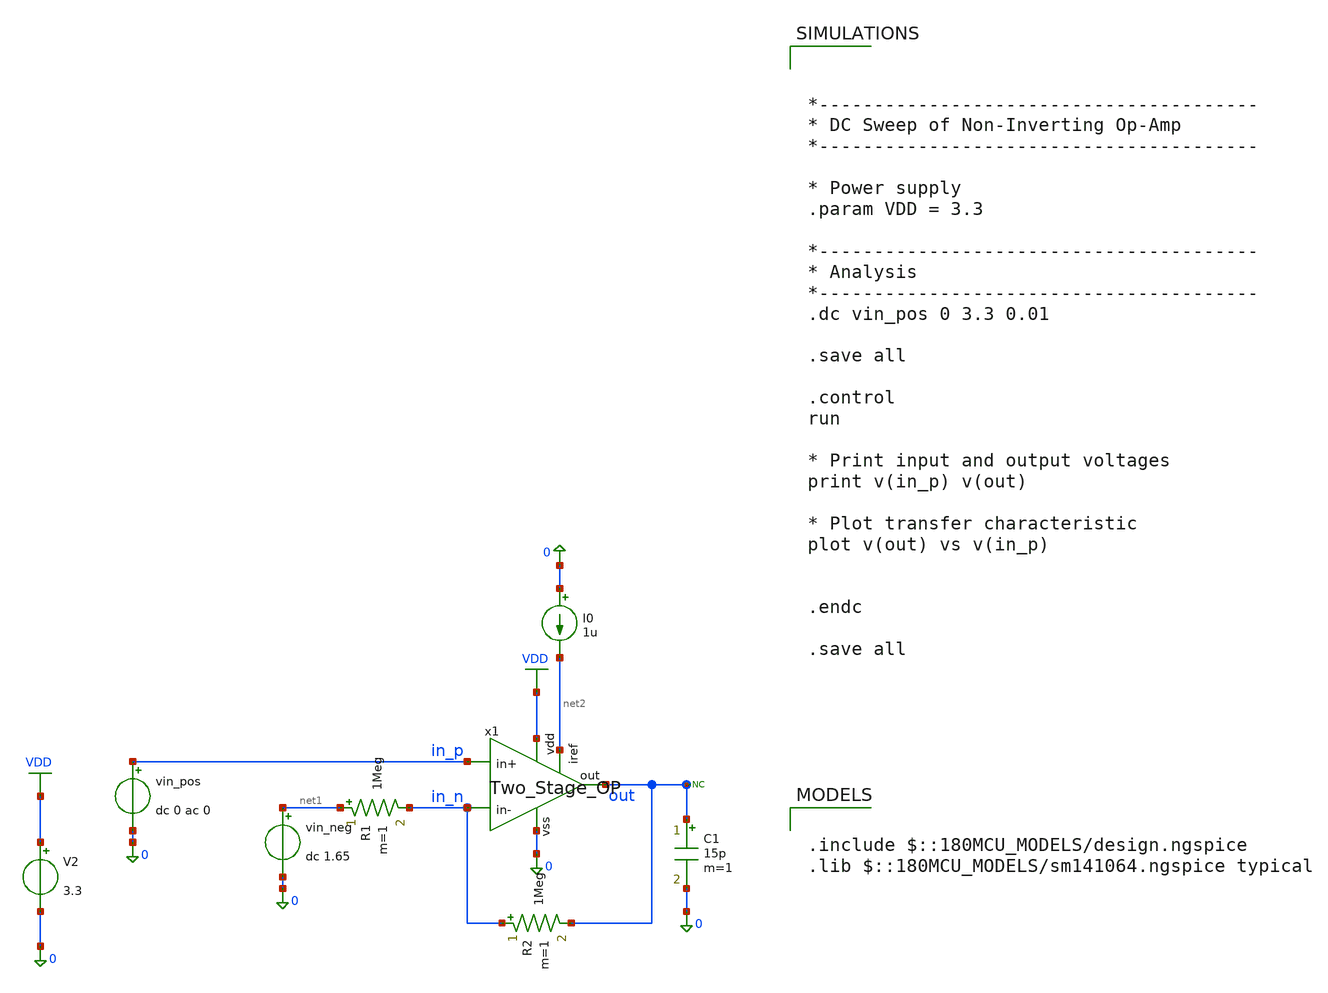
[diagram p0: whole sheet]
** sch_path: Marcel/designs/TB_NonInv_OP.sch
**.subckt TB_NonInv_OP
vin_pos in_p 0 dc 0 ac 0
V2 VDD 0 3.3
.save i(v2)
* noconn out
vin_neg net1 0 dc 1.65
C1 out 0 15p m=1
R1 net1 in_n 1Meg m=1
R2 in_n out 1Meg m=1
x1 out in_n in_p VDD 0 net2 Two_Stage_OP
I0 0 net2 1u
**** begin user architecture code

.include $::180MCU_MODELS/design.ngspice
.lib $::180MCU_MODELS/sm141064.ngspice typical




*----------------------------------------
* DC Sweep of Non-Inverting Op-Amp
*----------------------------------------

* Power supply
.param VDD = 3.3

*----------------------------------------
* Analysis
*----------------------------------------
.dc vin_pos 0 3.3 0.01

.save all

.control
run

* Print input and output voltages
print v(in_p) v(out)

* Plot transfer characteristic
plot v(out) vs v(in_p)


.endc

.save all


**** end user architecture code
**.ends
.GLOBAL VDD
.end
